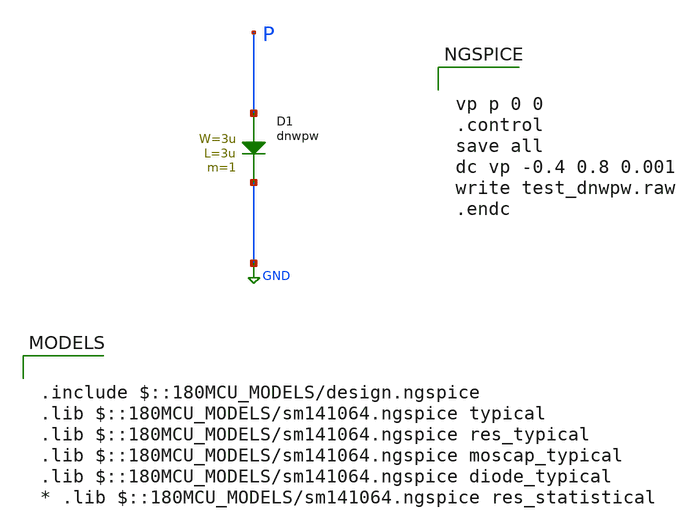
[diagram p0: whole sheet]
** sch_path: cells/xschem/tests/test_dnwpw.sch
* Copyright 2022 GlobalFoundries PDK Authors
* Licensed under the Apache License, Version 2.0 (the "License");
* you may not use this file except in compliance with the License.
* You may obtain a copy of the License at
* https://www.apache.org/licenses/LICENSE-2.0
* Unless required by applicable law or agreed to in writing, software
* distributed under the License is distributed on an "AS IS" BASIS,
* WITHOUT WARRANTIES OR CONDITIONS OF ANY KIND, either express or implied.
* See the License for the specific language governing permissions and
* limitations under the License.
**.subckt test_dnwpw
D1 P GND dnwpw area='3u * 3u ' pj='2*3u + 2*3u ' m=1
**** begin user architecture code

.include $::180MCU_MODELS/design.ngspice
.lib $::180MCU_MODELS/sm141064.ngspice typical
.lib $::180MCU_MODELS/sm141064.ngspice res_typical
.lib $::180MCU_MODELS/sm141064.ngspice moscap_typical
.lib $::180MCU_MODELS/sm141064.ngspice diode_typical
* .lib $::180MCU_MODELS/sm141064.ngspice res_statistical



vp p 0 0
.control
save all
dc vp -0.4 0.8 0.001
write test_dnwpw.raw
.endc


**** end user architecture code
**.ends
.GLOBAL GND
.end
